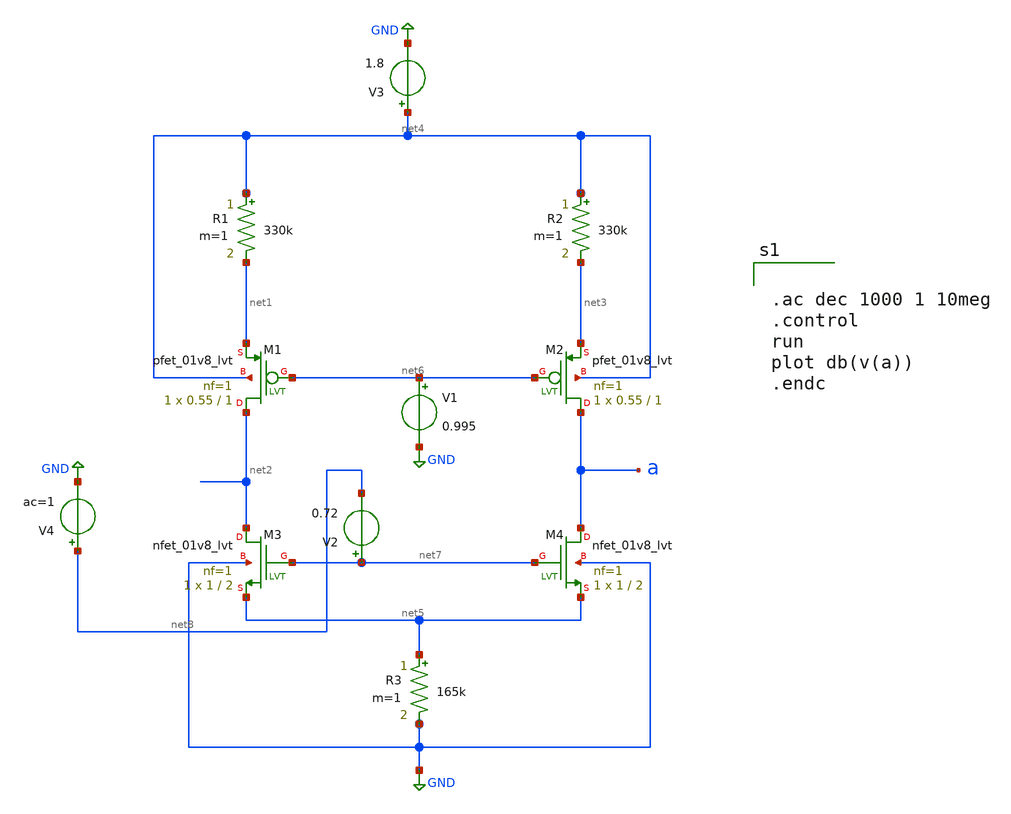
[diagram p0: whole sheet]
** sch_path: botop.sch
**.subckt botop
XM1 net2 net6 net1 net4 sky130_fd_pr__pfet_01v8_lvt L=1 W=0.55 nf=1 ad='int((nf+1)/2) * W/nf * 0.29'
+ as='int((nf+2)/2) * W/nf * 0.29' pd='2*int((nf+1)/2) * (W/nf + 0.29)' ps='2*int((nf+2)/2) * (W/nf + 0.29)'
+ nrd='0.29 / W' nrs='0.29 / W' sa=0 sb=0 sd=0 mult=1 m=1
XM2 a net6 net3 net4 sky130_fd_pr__pfet_01v8_lvt L=1 W=0.55 nf=1 ad='int((nf+1)/2) * W/nf * 0.29' as='int((nf+2)/2) * W/nf * 0.29'
+ pd='2*int((nf+1)/2) * (W/nf + 0.29)' ps='2*int((nf+2)/2) * (W/nf + 0.29)' nrd='0.29 / W' nrs='0.29 / W'
+ sa=0 sb=0 sd=0 mult=1 m=1
XM3 net2 net7 net5 GND sky130_fd_pr__nfet_01v8_lvt L=2 W=1 nf=1 ad='int((nf+1)/2) * W/nf * 0.29' as='int((nf+2)/2) * W/nf * 0.29'
+ pd='2*int((nf+1)/2) * (W/nf + 0.29)' ps='2*int((nf+2)/2) * (W/nf + 0.29)' nrd='0.29 / W' nrs='0.29 / W'
+ sa=0 sb=0 sd=0 mult=1 m=1
XM4 a net7 net5 GND sky130_fd_pr__nfet_01v8_lvt L=2 W=1 nf=1 ad='int((nf+1)/2) * W/nf * 0.29' as='int((nf+2)/2) * W/nf * 0.29'
+ pd='2*int((nf+1)/2) * (W/nf + 0.29)' ps='2*int((nf+2)/2) * (W/nf + 0.29)' nrd='0.29 / W' nrs='0.29 / W'
+ sa=0 sb=0 sd=0 mult=1 m=1
R1 net4 net1 330k m=1
R2 net4 net3 330k m=1
R3 net5 GND 165k m=1
V1 net6 GND 0.995
V3 net4 GND 1.8
V2 net7 net8 0.72
V4 net8 GND ac=1
**** begin user architecture code


.ac dec 1000 1 10meg
.control
run
plot db(v(a))
.endc


*.lib ~/open_pdks/sky130/sky130A/libs.tech/ngspice/sky130.lib.spice tt
.param mc_mm_switch=0
.param mc_pr_switch=0

.include ~/open_pdks/sky130/sky130A/libs.tech/ngspice/corners/tt/nonfet.spice


*model
.include ~/open_pdks/sky130/sky130A/libs.tech/ngspice/all.spice

*mosfet
.include ~/open_pdks/sky130/sky130A/libs.ref/sky130_fd_pr/spice/sky130_fd_pr__pfet_01v8_lvt__tt.corner.spice
.inclued ~/open_pdks/sky130/sky130A/libs.ref/sky130_fd_pr/spice/sky130_fd_pr__nfet_01v8_lvt__tt.corner.spice

*mismatch parameters
.include ~/open_pdks/sky130/sky130A/libs.ref/sky130_fd_pr/spice/sky130_fd_pr__pfet_01v8_lvt__mismatch.corner.spice
.include ~/open_pdks/sky130/sky130A/libs.ref/sky130_fd_pr/spice/sky130_fd_pr__nfet_01v8_lvt__mismatch.corner.spice

**** end user architecture code
**.ends
.GLOBAL GND
.end
